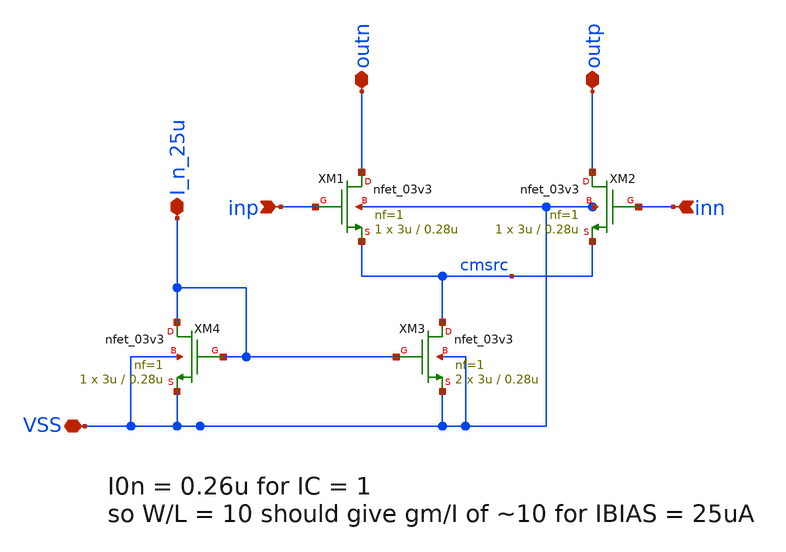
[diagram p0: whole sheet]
** sch_path: designs/libs/sandbox/dif_pair_nMOS.sch
**.subckt dif_pair_nMOS outn outp I_n_25u inp inn VSS
*.iopin outn
*.iopin outp
*.iopin I_n_25u
*.ipin inp
*.ipin inn
*.iopin VSS
XM1 outn inp cmsrc VSS nfet_03v3 L=0.28u W=3u nf=1 ad='int((nf+1)/2) * W/nf * 0.18u' as='int((nf+2)/2) * W/nf * 0.18u'
+ pd='2*int((nf+1)/2) * (W/nf + 0.18u)' ps='2*int((nf+2)/2) * (W/nf + 0.18u)' nrd='0.18u / W' nrs='0.18u / W'
+ sa=0 sb=0 sd=0 m=1
XM2 outp inn cmsrc VSS nfet_03v3 L=0.28u W=3u nf=1 ad='int((nf+1)/2) * W/nf * 0.18u' as='int((nf+2)/2) * W/nf * 0.18u'
+ pd='2*int((nf+1)/2) * (W/nf + 0.18u)' ps='2*int((nf+2)/2) * (W/nf + 0.18u)' nrd='0.18u / W' nrs='0.18u / W'
+ sa=0 sb=0 sd=0 m=1
XM3 cmsrc I_n_25u VSS VSS nfet_03v3 L=0.28u W=3u nf=1 ad='int((nf+1)/2) * W/nf * 0.18u' as='int((nf+2)/2) * W/nf * 0.18u'
+ pd='2*int((nf+1)/2) * (W/nf + 0.18u)' ps='2*int((nf+2)/2) * (W/nf + 0.18u)' nrd='0.18u / W' nrs='0.18u / W'
+ sa=0 sb=0 sd=0 m=2
XM4 I_n_25u I_n_25u VSS VSS nfet_03v3 L=0.28u W=3u nf=1 ad='int((nf+1)/2) * W/nf * 0.18u' as='int((nf+2)/2) * W/nf * 0.18u'
+ pd='2*int((nf+1)/2) * (W/nf + 0.18u)' ps='2*int((nf+2)/2) * (W/nf + 0.18u)' nrd='0.18u / W' nrs='0.18u / W'
+ sa=0 sb=0 sd=0 m=1
**.ends
.end
